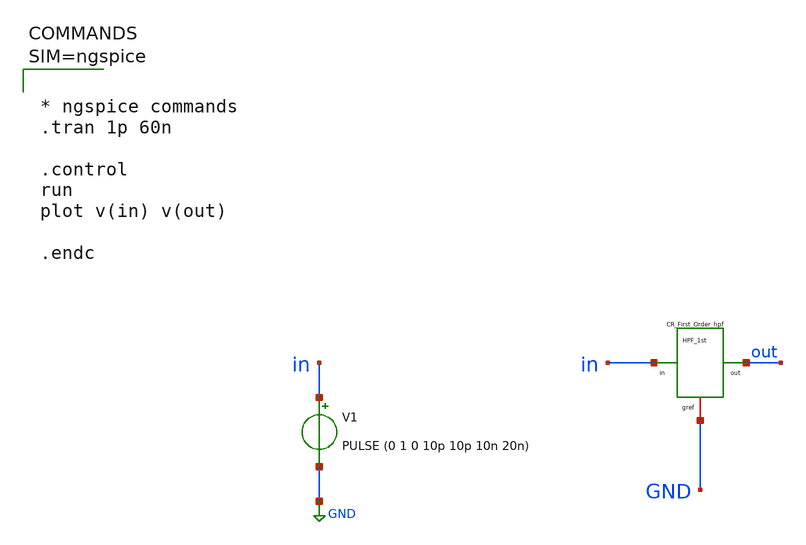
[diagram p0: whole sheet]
** sch_path: sch/tb_CR_hpf.sch
**.subckt tb_CR_hpf
V1 in GND PULSE (0 1 0 10p 10p 10n 20n)
x1 in out GND CR_First_Order_hpf
**** begin user architecture code



* ngspice commands
.tran 1p 60n

.control
run
plot v(in) v(out)

.endc



**** end user architecture code
**.ends

* expanding   symbol:  CR_First_Order_hpf.sym # of pins=3
** sym_path: sch/CR_First_Order_hpf.sym
** sch_path: sch/CR_First_Order_hpf.sch
.subckt CR_First_Order_hpf in out gref
*.ipin in
*.iopin gref
*.opin out
R1 out gref 1k m=1
C1 in out 1p m=1
.ends

.GLOBAL GND
.end
